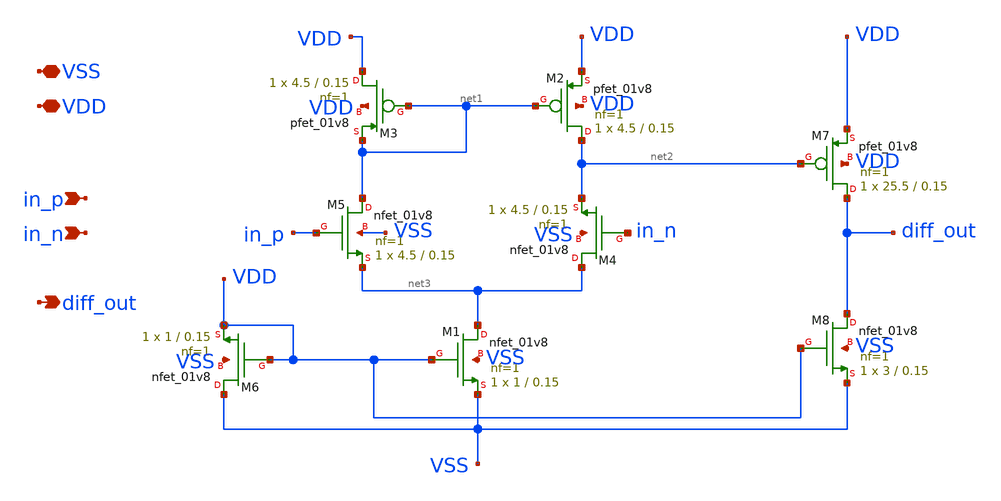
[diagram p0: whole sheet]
** sch_path: xschem/src/Hw2amp.sch
**.subckt Hw2amp in_p VDD diff_out in_n VSS
*.ipin in_p
*.iopin VDD
*.opin diff_out
*.ipin in_n
*.iopin VSS
XM1 net3 VDD VSS VSS sky130_fd_pr__nfet_01v8 L=0.15 W=1 nf=1 ad='int((nf+1)/2) * W/nf * 0.29' as='int((nf+2)/2) * W/nf * 0.29'
+ pd='2*int((nf+1)/2) * (W/nf + 0.29)' ps='2*int((nf+2)/2) * (W/nf + 0.29)' nrd='0.29 / W' nrs='0.29 / W'
+ sa=0 sb=0 sd=0 mult=1 m=1
XM2 net2 net1 VDD VDD sky130_fd_pr__pfet_01v8 L=0.15 W=4.5 nf=1 ad='int((nf+1)/2) * W/nf * 0.29' as='int((nf+2)/2) * W/nf * 0.29'
+ pd='2*int((nf+1)/2) * (W/nf + 0.29)' ps='2*int((nf+2)/2) * (W/nf + 0.29)' nrd='0.29 / W' nrs='0.29 / W'
+ sa=0 sb=0 sd=0 mult=1 m=1
XM3 VDD net1 net1 VDD sky130_fd_pr__pfet_01v8 L=0.15 W=4.5 nf=1 ad='int((nf+1)/2) * W/nf * 0.29' as='int((nf+2)/2) * W/nf * 0.29'
+ pd='2*int((nf+1)/2) * (W/nf + 0.29)' ps='2*int((nf+2)/2) * (W/nf + 0.29)' nrd='0.29 / W' nrs='0.29 / W'
+ sa=0 sb=0 sd=0 mult=1 m=1
XM4 net3 in_n net2 VSS sky130_fd_pr__nfet_01v8 L=0.15 W=4.5 nf=1 ad='int((nf+1)/2) * W/nf * 0.29' as='int((nf+2)/2) * W/nf * 0.29'
+ pd='2*int((nf+1)/2) * (W/nf + 0.29)' ps='2*int((nf+2)/2) * (W/nf + 0.29)' nrd='0.29 / W' nrs='0.29 / W'
+ sa=0 sb=0 sd=0 mult=1 m=1
XM5 net1 in_p net3 VSS sky130_fd_pr__nfet_01v8 L=0.15 W=4.5 nf=1 ad='int((nf+1)/2) * W/nf * 0.29' as='int((nf+2)/2) * W/nf * 0.29'
+ pd='2*int((nf+1)/2) * (W/nf + 0.29)' ps='2*int((nf+2)/2) * (W/nf + 0.29)' nrd='0.29 / W' nrs='0.29 / W'
+ sa=0 sb=0 sd=0 mult=1 m=1
XM6 VSS VDD VDD VSS sky130_fd_pr__nfet_01v8 L=0.15 W=1 nf=1 ad='int((nf+1)/2) * W/nf * 0.29' as='int((nf+2)/2) * W/nf * 0.29'
+ pd='2*int((nf+1)/2) * (W/nf + 0.29)' ps='2*int((nf+2)/2) * (W/nf + 0.29)' nrd='0.29 / W' nrs='0.29 / W'
+ sa=0 sb=0 sd=0 mult=1 m=1
XM7 diff_out net2 VDD VDD sky130_fd_pr__pfet_01v8 L=0.15 W=25.5 nf=1 ad='int((nf+1)/2) * W/nf * 0.29'
+ as='int((nf+2)/2) * W/nf * 0.29' pd='2*int((nf+1)/2) * (W/nf + 0.29)' ps='2*int((nf+2)/2) * (W/nf + 0.29)'
+ nrd='0.29 / W' nrs='0.29 / W' sa=0 sb=0 sd=0 mult=1 m=1
XM8 diff_out VDD VSS VSS sky130_fd_pr__nfet_01v8 L=0.15 W=3 nf=1 ad='int((nf+1)/2) * W/nf * 0.29' as='int((nf+2)/2) * W/nf * 0.29'
+ pd='2*int((nf+1)/2) * (W/nf + 0.29)' ps='2*int((nf+2)/2) * (W/nf + 0.29)' nrd='0.29 / W' nrs='0.29 / W'
+ sa=0 sb=0 sd=0 mult=1 m=1
**** begin user architecture code


**** end user architecture code
**.ends
.end
